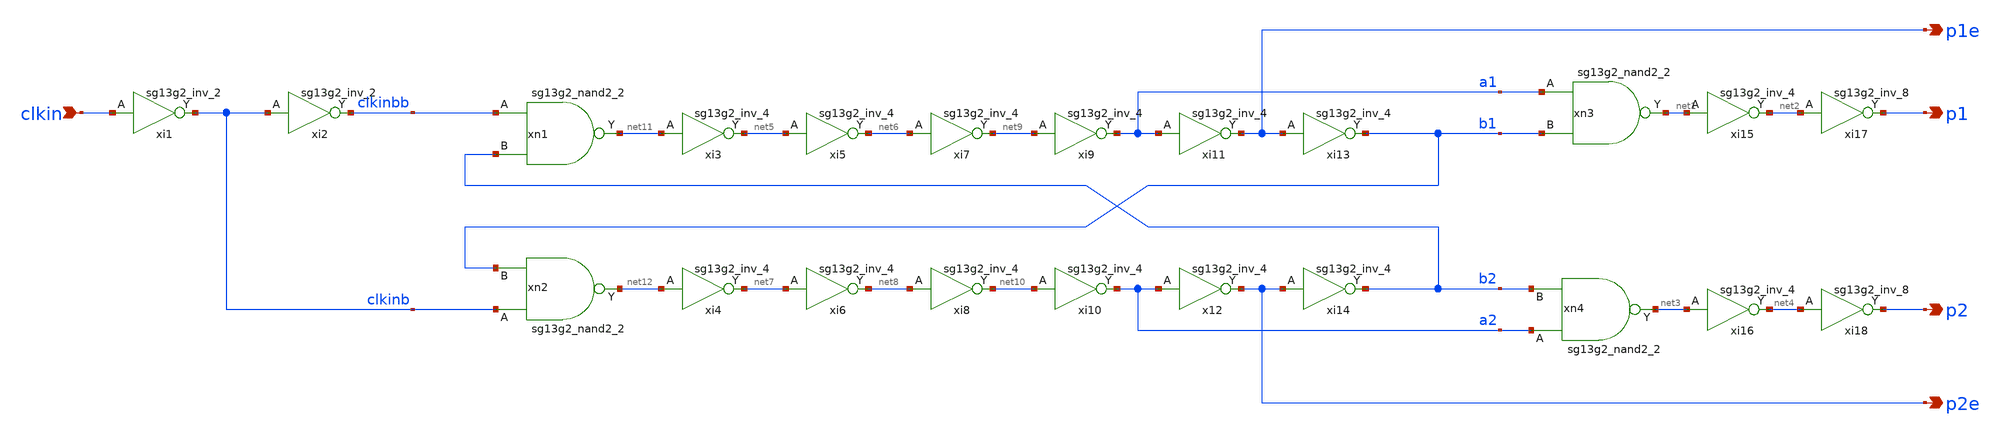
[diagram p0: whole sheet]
** sch_path: DSM/Schematics/CLK_design_hanieh/3_Real_circuits/template_clkgen.sch
* IHP-GmbH/IHP-Open-PDK/ihp-sg13g2/libs.tech/xschem/sg13g2_stdcells/sg13g2_inv_2.sch:
* Copyright 2023 IHP PDK Authors
* Licensed under the Apache License, Version 2.0 (the "License");
**.subckt template_clkgen clkin p1e p1 p2 p2e
*.ipin clkin
*.opin p1e
*.opin p1
*.opin p2
*.opin p2e
xn1 net11 clkinbb b2 VDD VSS sg13g2_nand2_2
xi7 net9 net6 VDD VSS sg13g2_inv_4
xi1 clkinb clkin VDD VSS sg13g2_inv_2
xi2 clkinbb clkinb VDD VSS sg13g2_inv_2
xn2 net12 clkinb b1 VDD VSS sg13g2_nand2_2
xi13 b1 p1e VDD VSS sg13g2_inv_4
xi8 net10 net8 VDD VSS sg13g2_inv_4
xi14 b2 p2e VDD VSS sg13g2_inv_4
xn3 net1 a1 b1 VDD VSS sg13g2_nand2_2
xn4 net3 a2 b2 VDD VSS sg13g2_nand2_2
xi11 p1e a1 VDD VSS sg13g2_inv_4
xi9 a1 net9 VDD VSS sg13g2_inv_4
x12 p2e a2 VDD VSS sg13g2_inv_4
xi10 a2 net10 VDD VSS sg13g2_inv_4
xi15 net2 net1 VDD VSS sg13g2_inv_4
xi17 p1 net2 VDD VSS sg13g2_inv_8
xi16 net4 net3 VDD VSS sg13g2_inv_4
xi18 p2 net4 VDD VSS sg13g2_inv_8
xi3 net5 net11 VDD VSS sg13g2_inv_4
xi5 net6 net5 VDD VSS sg13g2_inv_4
xi4 net7 net12 VDD VSS sg13g2_inv_4
xi6 net8 net7 VDD VSS sg13g2_inv_4
**.ends

* expanding   symbol:  sg13g2_stdcells/sg13g2_nand2_2.sym # of pins=3
** sym_path: sg13g2_stdcells/sg13g2_nand2_2.sym
** sch_path: sg13g2_stdcells/sg13g2_nand2_2.sch
.subckt sg13g2_nand2_2 Y A B VDD VSS
*.iopin VDD
*.iopin VSS
*.opin Y
*.ipin B
*.ipin A
XM1 Y A net1 VSS sg13_lv_nmos w=1.44u l=130.00n ng=2 m=1 mm_ok=1
XM2 net1 B VSS VSS sg13_lv_nmos w=1.44u l=130.00n ng=2 m=1 mm_ok=1
XM3 Y A VDD VDD sg13_lv_pmos w=2.24u l=130.00n ng=2 m=1 mm_ok=1
XM4 Y B VDD VDD sg13_lv_pmos w=2.24u l=130.00n ng=2 m=1 mm_ok=1
.ends


* expanding   symbol:  sg13g2_stdcells/sg13g2_inv_4.sym # of pins=2
** sym_path: sg13g2_stdcells/sg13g2_inv_4.sym
** sch_path: sg13g2_stdcells/sg13g2_inv_4.sch
.subckt sg13g2_inv_4 Y A VDD VSS
*.ipin A
*.opin Y
*.iopin VDD
*.iopin VSS
XM1 Y A VSS VSS sg13_lv_nmos w=2.96u l=130.00n ng=4 m=1 mm_ok=1
XM2 Y A VDD VDD sg13_lv_pmos w=4.48u l=130.00n ng=4 m=1 mm_ok=1
.ends


* expanding   symbol:  sg13g2_stdcells/sg13g2_inv_2.sym # of pins=2
** sym_path: sg13g2_stdcells/sg13g2_inv_2.sym
** sch_path: sg13g2_stdcells/sg13g2_inv_2.sch
.subckt sg13g2_inv_2 Y A VDD VSS
*.opin Y
*.ipin A
*.iopin VDD
*.iopin VSS
XM1 Y A VSS VSS sg13_lv_nmos w=1.48u l=130.00n ng=2 m=1 mm_ok=1
XM2 Y A VDD VDD sg13_lv_pmos w=2.24u l=130.00n ng=2 m=1 mm_ok=1
.ends


* expanding   symbol:  sg13g2_stdcells/sg13g2_inv_8.sym # of pins=2
** sym_path: sg13g2_stdcells/sg13g2_inv_8.sym
** sch_path: sg13g2_stdcells/sg13g2_inv_8.sch
.subckt sg13g2_inv_8 Y A VDD VSS
*.opin Y
*.ipin A
*.iopin VDD
*.iopin VSS
XM1 Y A VSS VSS sg13_lv_nmos w=5.92u l=130.00n ng=8 m=1 mm_ok=1
XM2 Y A VDD VDD sg13_lv_pmos w=8.96u l=130.00n ng=8 m=1 mm_ok=1
.ends

.end
